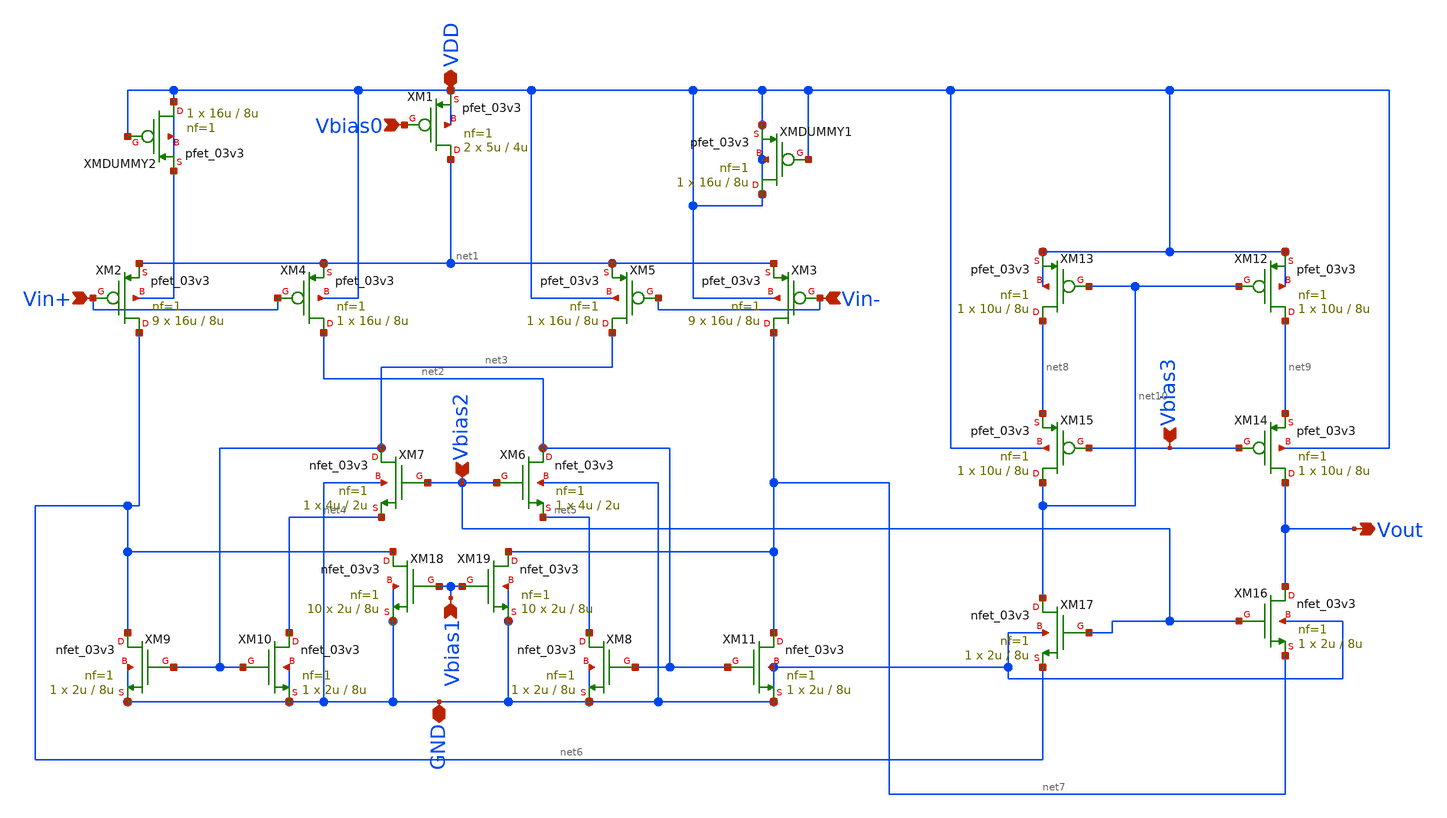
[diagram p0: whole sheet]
** sch_path: analog/B04_LNA_OTA.sch
**.subckt B04_LNA_OTA VDD Vbias0 Vin+ Vin- Vout Vbias3 Vbias2 GND Vbias1
*.iopin VDD
*.ipin Vbias0
*.ipin Vin+
*.ipin Vin-
*.opin Vout
*.ipin Vbias3
*.ipin Vbias2
*.iopin GND
*.ipin Vbias1
XM1 net1 Vbias0 VDD VDD pfet_03v3 L=4u W=5u nf=1 ad='int((nf+1)/2) * W/nf * 0.18u' as='int((nf+2)/2) * W/nf * 0.18u'
+ pd='2*int((nf+1)/2) * (W/nf + 0.18u)' ps='2*int((nf+2)/2) * (W/nf + 0.18u)' nrd='0.18u / W' nrs='0.18u / W'
+ sa=0 sb=0 sd=0 m=2
XM2 net6 Vin+ net1 VDD pfet_03v3 L=8u W=16u nf=1 ad='int((nf+1)/2) * W/nf * 0.18u' as='int((nf+2)/2) * W/nf * 0.18u'
+ pd='2*int((nf+1)/2) * (W/nf + 0.18u)' ps='2*int((nf+2)/2) * (W/nf + 0.18u)' nrd='0.18u / W' nrs='0.18u / W'
+ sa=0 sb=0 sd=0 m=9
XM3 net7 Vin- net1 VDD pfet_03v3 L=8u W=16u nf=1 ad='int((nf+1)/2) * W/nf * 0.18u' as='int((nf+2)/2) * W/nf * 0.18u'
+ pd='2*int((nf+1)/2) * (W/nf + 0.18u)' ps='2*int((nf+2)/2) * (W/nf + 0.18u)' nrd='0.18u / W' nrs='0.18u / W'
+ sa=0 sb=0 sd=0 m=9
XM4 net2 Vin+ net1 VDD pfet_03v3 L=8u W=16u nf=1 ad='int((nf+1)/2) * W/nf * 0.18u' as='int((nf+2)/2) * W/nf * 0.18u'
+ pd='2*int((nf+1)/2) * (W/nf + 0.18u)' ps='2*int((nf+2)/2) * (W/nf + 0.18u)' nrd='0.18u / W' nrs='0.18u / W'
+ sa=0 sb=0 sd=0 m=1
XM5 net3 Vin- net1 VDD pfet_03v3 L=8u W=16u nf=1 ad='int((nf+1)/2) * W/nf * 0.18u' as='int((nf+2)/2) * W/nf * 0.18u'
+ pd='2*int((nf+1)/2) * (W/nf + 0.18u)' ps='2*int((nf+2)/2) * (W/nf + 0.18u)' nrd='0.18u / W' nrs='0.18u / W'
+ sa=0 sb=0 sd=0 m=1
XM6 net2 Vbias2 net5 GND nfet_03v3 L=2u W=4u nf=1 ad='int((nf+1)/2) * W/nf * 0.18u' as='int((nf+2)/2) * W/nf * 0.18u'
+ pd='2*int((nf+1)/2) * (W/nf + 0.18u)' ps='2*int((nf+2)/2) * (W/nf + 0.18u)' nrd='0.18u / W' nrs='0.18u / W'
+ sa=0 sb=0 sd=0 m=1
XM7 net3 Vbias2 net4 GND nfet_03v3 L=2u W=4u nf=1 ad='int((nf+1)/2) * W/nf * 0.18u' as='int((nf+2)/2) * W/nf * 0.18u'
+ pd='2*int((nf+1)/2) * (W/nf + 0.18u)' ps='2*int((nf+2)/2) * (W/nf + 0.18u)' nrd='0.18u / W' nrs='0.18u / W'
+ sa=0 sb=0 sd=0 m=1
XM8 net5 net2 GND GND nfet_03v3 L=8u W=2u nf=1 ad='int((nf+1)/2) * W/nf * 0.18u' as='int((nf+2)/2) * W/nf * 0.18u'
+ pd='2*int((nf+1)/2) * (W/nf + 0.18u)' ps='2*int((nf+2)/2) * (W/nf + 0.18u)' nrd='0.18u / W' nrs='0.18u / W'
+ sa=0 sb=0 sd=0 m=1
XM9 net6 net3 GND GND nfet_03v3 L=8u W=2u nf=1 ad='int((nf+1)/2) * W/nf * 0.18u' as='int((nf+2)/2) * W/nf * 0.18u'
+ pd='2*int((nf+1)/2) * (W/nf + 0.18u)' ps='2*int((nf+2)/2) * (W/nf + 0.18u)' nrd='0.18u / W' nrs='0.18u / W'
+ sa=0 sb=0 sd=0 m=1
XM10 net4 net3 GND GND nfet_03v3 L=8u W=2u nf=1 ad='int((nf+1)/2) * W/nf * 0.18u' as='int((nf+2)/2) * W/nf * 0.18u'
+ pd='2*int((nf+1)/2) * (W/nf + 0.18u)' ps='2*int((nf+2)/2) * (W/nf + 0.18u)' nrd='0.18u / W' nrs='0.18u / W'
+ sa=0 sb=0 sd=0 m=1
XM11 net7 net2 GND GND nfet_03v3 L=8u W=2u nf=1 ad='int((nf+1)/2) * W/nf * 0.18u' as='int((nf+2)/2) * W/nf * 0.18u'
+ pd='2*int((nf+1)/2) * (W/nf + 0.18u)' ps='2*int((nf+2)/2) * (W/nf + 0.18u)' nrd='0.18u / W' nrs='0.18u / W'
+ sa=0 sb=0 sd=0 m=1
XM12 net9 net10 VDD VDD pfet_03v3 L=8u W=10u nf=1 ad='int((nf+1)/2) * W/nf * 0.18u' as='int((nf+2)/2) * W/nf * 0.18u'
+ pd='2*int((nf+1)/2) * (W/nf + 0.18u)' ps='2*int((nf+2)/2) * (W/nf + 0.18u)' nrd='0.18u / W' nrs='0.18u / W'
+ sa=0 sb=0 sd=0 m=1
XM13 net8 net10 VDD VDD pfet_03v3 L=8u W=10u nf=1 ad='int((nf+1)/2) * W/nf * 0.18u' as='int((nf+2)/2) * W/nf * 0.18u'
+ pd='2*int((nf+1)/2) * (W/nf + 0.18u)' ps='2*int((nf+2)/2) * (W/nf + 0.18u)' nrd='0.18u / W' nrs='0.18u / W'
+ sa=0 sb=0 sd=0 m=1
XM14 Vout Vbias3 net9 VDD pfet_03v3 L=8u W=10u nf=1 ad='int((nf+1)/2) * W/nf * 0.18u' as='int((nf+2)/2) * W/nf * 0.18u'
+ pd='2*int((nf+1)/2) * (W/nf + 0.18u)' ps='2*int((nf+2)/2) * (W/nf + 0.18u)' nrd='0.18u / W' nrs='0.18u / W'
+ sa=0 sb=0 sd=0 m=1
XM15 net10 Vbias3 net8 VDD pfet_03v3 L=8u W=10u nf=1 ad='int((nf+1)/2) * W/nf * 0.18u' as='int((nf+2)/2) * W/nf * 0.18u'
+ pd='2*int((nf+1)/2) * (W/nf + 0.18u)' ps='2*int((nf+2)/2) * (W/nf + 0.18u)' nrd='0.18u / W' nrs='0.18u / W'
+ sa=0 sb=0 sd=0 m=1
XM16 Vout Vbias2 net7 GND nfet_03v3 L=8u W=2u nf=1 ad='int((nf+1)/2) * W/nf * 0.18u' as='int((nf+2)/2) * W/nf * 0.18u'
+ pd='2*int((nf+1)/2) * (W/nf + 0.18u)' ps='2*int((nf+2)/2) * (W/nf + 0.18u)' nrd='0.18u / W' nrs='0.18u / W'
+ sa=0 sb=0 sd=0 m=1
XM17 net10 Vbias2 net6 GND nfet_03v3 L=8u W=2u nf=1 ad='int((nf+1)/2) * W/nf * 0.18u' as='int((nf+2)/2) * W/nf * 0.18u'
+ pd='2*int((nf+1)/2) * (W/nf + 0.18u)' ps='2*int((nf+2)/2) * (W/nf + 0.18u)' nrd='0.18u / W' nrs='0.18u / W'
+ sa=0 sb=0 sd=0 m=1
XM18 net6 Vbias1 GND GND nfet_03v3 L=8u W=2u nf=1 ad='int((nf+1)/2) * W/nf * 0.18u' as='int((nf+2)/2) * W/nf * 0.18u'
+ pd='2*int((nf+1)/2) * (W/nf + 0.18u)' ps='2*int((nf+2)/2) * (W/nf + 0.18u)' nrd='0.18u / W' nrs='0.18u / W'
+ sa=0 sb=0 sd=0 m=10
XM19 net7 Vbias1 GND GND nfet_03v3 L=8u W=2u nf=1 ad='int((nf+1)/2) * W/nf * 0.18u' as='int((nf+2)/2) * W/nf * 0.18u'
+ pd='2*int((nf+1)/2) * (W/nf + 0.18u)' ps='2*int((nf+2)/2) * (W/nf + 0.18u)' nrd='0.18u / W' nrs='0.18u / W'
+ sa=0 sb=0 sd=0 m=10
XMDUMMY1 VDD VDD VDD VDD pfet_03v3 L=8u W=16u nf=1 ad='int((nf+1)/2) * W/nf * 0.18u' as='int((nf+2)/2) * W/nf * 0.18u'
+ pd='2*int((nf+1)/2) * (W/nf + 0.18u)' ps='2*int((nf+2)/2) * (W/nf + 0.18u)' nrd='0.18u / W' nrs='0.18u / W'
+ sa=0 sb=0 sd=0 m=1
XMDUMMY2 VDD VDD VDD VDD pfet_03v3 L=8u W=16u nf=1 ad='int((nf+1)/2) * W/nf * 0.18u' as='int((nf+2)/2) * W/nf * 0.18u'
+ pd='2*int((nf+1)/2) * (W/nf + 0.18u)' ps='2*int((nf+2)/2) * (W/nf + 0.18u)' nrd='0.18u / W' nrs='0.18u / W'
+ sa=0 sb=0 sd=0 m=1
**.ends
.end
